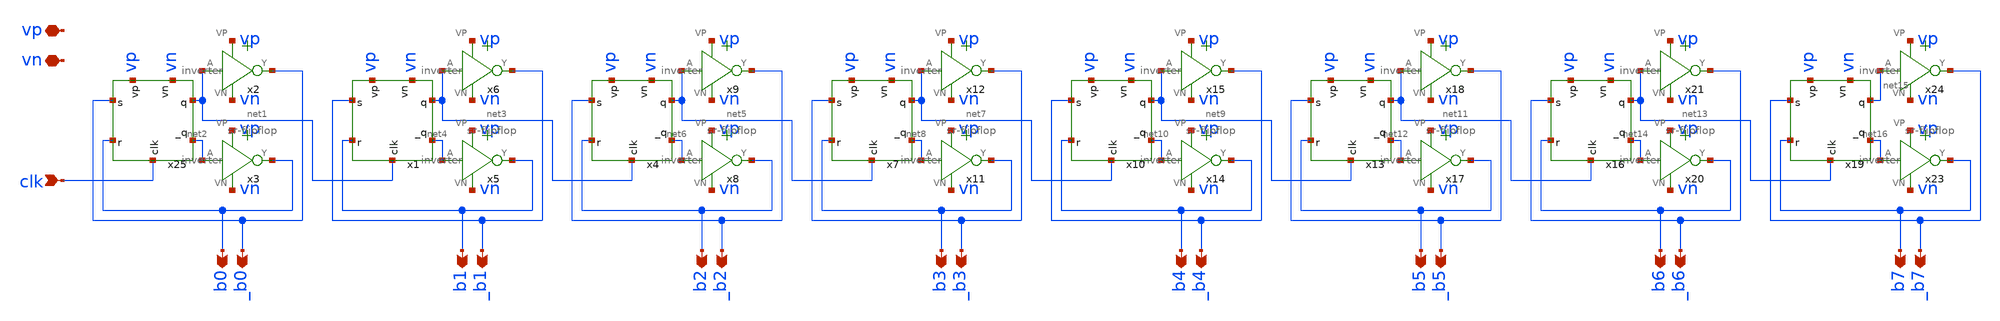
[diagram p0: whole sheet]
** sch_path: xschem/logic_gates/counter.sch
**.subckt counter vp vn clk b0 _b0 b1 _b1 b2 _b2 b3 _b3 b4 _b4 b5 _b5 b6 _b6 b7 _b7
*.iopin vp
*.iopin vn
*.ipin clk
*.opin b0
*.opin _b0
*.opin b1
*.opin _b1
*.opin b2
*.opin _b2
*.opin b3
*.opin _b3
*.opin b4
*.opin _b4
*.opin b5
*.opin _b5
*.opin b6
*.opin _b6
*.opin b7
*.opin _b7
x3 vp net2 b0 vn inverter
x2 vp net1 _b0 vn inverter
x5 vp net4 b1 vn inverter
x6 vp net3 _b1 vn inverter
x8 vp net6 b2 vn inverter
x9 vp net5 _b2 vn inverter
x11 vp net8 b3 vn inverter
x12 vp net7 _b3 vn inverter
x14 vp net10 b4 vn inverter
x15 vp net9 _b4 vn inverter
x17 vp net12 b5 vn inverter
x18 vp net11 _b5 vn inverter
x20 vp net14 b6 vn inverter
x21 vp net13 _b6 vn inverter
x23 vp net16 b7 vn inverter
x24 vp net15 _b7 vn inverter
x25 vp vn _b0 net1 b0 net2 clk sr-flipflop
x1 vp vn _b1 net3 b1 net4 net1 sr-flipflop
x4 vp vn _b2 net5 b2 net6 net3 sr-flipflop
x7 vp vn _b3 net7 b3 net8 net5 sr-flipflop
x10 vp vn _b4 net9 b4 net10 net7 sr-flipflop
x13 vp vn _b5 net11 b5 net12 net9 sr-flipflop
x16 vp vn _b6 net13 b6 net14 net11 sr-flipflop
x19 vp vn _b7 net15 b7 net16 net13 sr-flipflop
**.ends
.end
